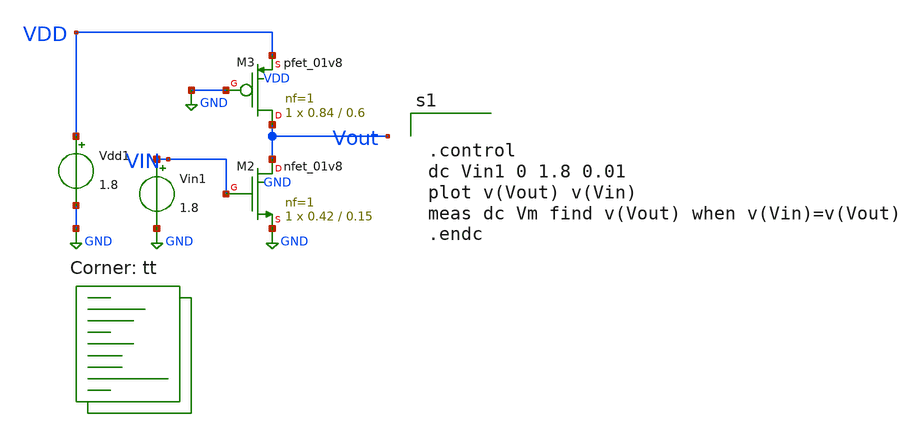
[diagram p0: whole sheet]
** sch_path: tutorial_3/tutorial_3_2a.sch
**.subckt tutorial_3_2a
XM2 Vout VIN GND GND sky130_fd_pr__nfet_01v8 L=0.15 W=0.42 nf=1 ad='int((nf+1)/2) * W/nf * 0.29' as='int((nf+2)/2) * W/nf * 0.29'
+ pd='2*int((nf+1)/2) * (W/nf + 0.29)' ps='2*int((nf+2)/2) * (W/nf + 0.29)' nrd='0.29 / W' nrs='0.29 / W'
+ sa=0 sb=0 sd=0 mult=1 m=1
XM3 Vout GND VDD VDD sky130_fd_pr__pfet_01v8 L=0.6 W=0.84 nf=1 ad='int((nf+1)/2) * W/nf * 0.29' as='int((nf+2)/2) * W/nf * 0.29'
+ pd='2*int((nf+1)/2) * (W/nf + 0.29)' ps='2*int((nf+2)/2) * (W/nf + 0.29)' nrd='0.29 / W' nrs='0.29 / W'
+ sa=0 sb=0 sd=0 mult=1 m=1
Vin1 VIN GND 1.8
Vdd1 VDD GND 1.8
**** begin user architecture code
.lib $::SKYWATER_MODELS/sky130.lib.spice tt


.control
dc Vin1 0 1.8 0.01
plot v(Vout) v(Vin)
meas dc Vm find v(Vout) when v(Vin)=v(Vout)
.endc

**** end user architecture code
**.ends
.GLOBAL GND
.end
